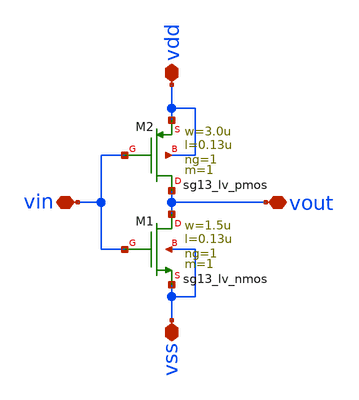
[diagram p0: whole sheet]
** sch_path: xschem/inverter.sch
**.subckt inverter vout vss vin vdd
*.iopin vout
*.iopin vss
*.iopin vin
*.iopin vdd
XM1 vout vin vss vss sg13_lv_nmos w=1.5u l=0.13u ng=1 m=1 mm_ok=1
XM2 vout vin vdd vdd sg13_lv_pmos w=3.0u l=0.13u ng=1 m=1 mm_ok=1
**.ends
.end
